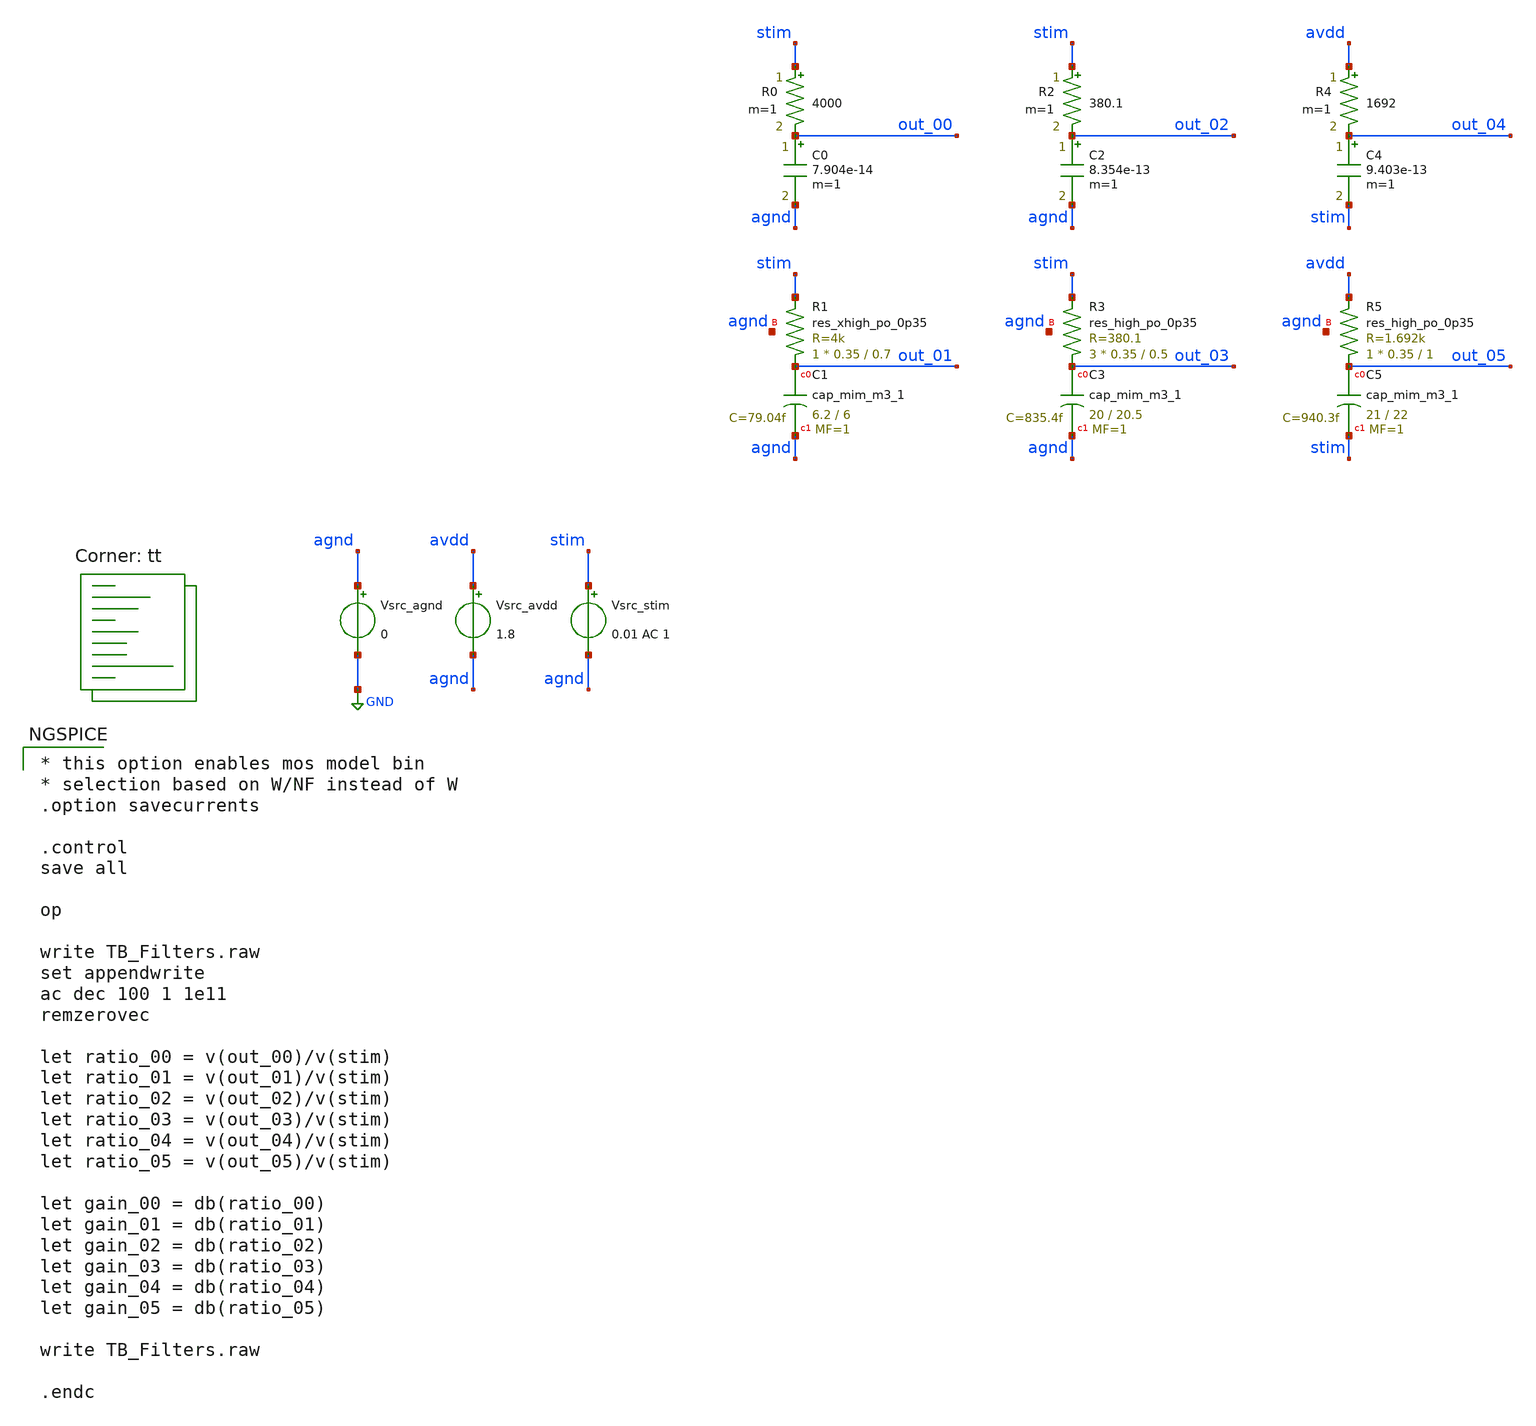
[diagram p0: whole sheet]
** sch_path: LPF/TB_Filters.sch
**.subckt TB_Filters
Vsrc_agnd agnd GND 0
Vsrc_stim stim agnd 0.01 AC 1
XC1 out_01 agnd sky130_fd_pr__cap_mim_m3_1 W=6.2 L=6 MF=1 m=1
XR1 out_01 stim agnd sky130_fd_pr__res_xhigh_po_0p35 L=0.7 mult=1 m=1
R0 stim out_00 4000 m=1
C0 out_00 agnd 7.904e-14 m=1
XC3 out_03 agnd sky130_fd_pr__cap_mim_m3_1 W=20 L=20.5 MF=1 m=1
R2 stim out_02 380.1 m=1
C2 out_02 agnd 8.354e-13 m=1
XR3 out_03 stim agnd sky130_fd_pr__res_high_po_0p35 L=0.5 mult=3 m=3
Vsrc_avdd avdd agnd 1.8
R4 avdd out_04 1692 m=1
C4 out_04 stim 9.403e-13 m=1
XC5 out_05 stim sky130_fd_pr__cap_mim_m3_1 W=21 L=22 MF=1 m=1
XR5 out_05 avdd agnd sky130_fd_pr__res_high_po_0p35 L=1 mult=1 m=1
**** begin user architecture code
.lib $::SKYWATER_MODELS/sky130.lib.spice tt

* this option enables mos model bin
* selection based on W/NF instead of W
.option savecurrents

.control
save all

op

write TB_Filters.raw
set appendwrite
ac dec 100 1 1e11
remzerovec

let ratio_00 = v(out_00)/v(stim)
let ratio_01 = v(out_01)/v(stim)
let ratio_02 = v(out_02)/v(stim)
let ratio_03 = v(out_03)/v(stim)
let ratio_04 = v(out_04)/v(stim)
let ratio_05 = v(out_05)/v(stim)

let gain_00 = db(ratio_00)
let gain_01 = db(ratio_01)
let gain_02 = db(ratio_02)
let gain_03 = db(ratio_03)
let gain_04 = db(ratio_04)
let gain_05 = db(ratio_05)

write TB_Filters.raw

.endc


**** end user architecture code
**.ends
.GLOBAL GND
.end
